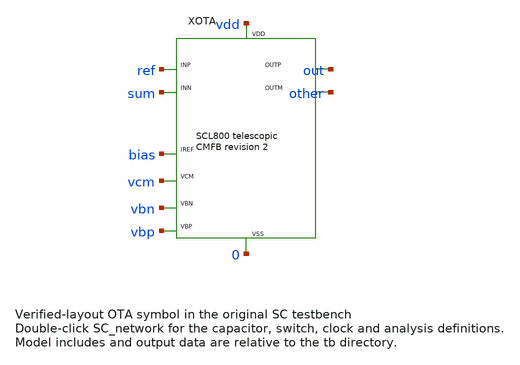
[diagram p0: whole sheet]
** sch_path: OTA/current_telescopic_cmfb_v2/designs/sc_ota_cmfb_v2.sch
**.subckt sc_ota_cmfb_v2
XOTA ref sum out other vdd 0 bias vcm vbn vbp ota_telescopic_cmfb_v2
**** begin user architecture code

.include /home/berson_meshak/pdk/scl08/ngspice_models49/mos/tntp49_5v
.include /home/berson_meshak/pdk/scl08/ngspice_models49/res/typ/ppr
.include ../models/ota_cmfb_v2_C.spice
.temp 27
.options reltol=1e-5 vntol=1e-8 abstol=1e-12 numdgt=12 method=gear maxord=2
VDD vdd 0 5
VREF ref 0 1.5
VP vp 0 0.3
IREF vdd bias 3.5u
CS tx rx 2.5p
CF sum out 7.5p
CL out 0 5p
VCM vcm 0 2.5
VBN vbn 0 2.4
VBP vbp vdd -2.2
COM other 0 5p
Vp1 p1 0 PWL(0 0 5.04e-05 0 5.041e-05 5 5.9e-05 5 5.901e-05 0 7.04e-05 0 7.041e-05 5 7.9e-05 5
+ 7.901e-05 0 9.04e-05 0 9.041e-05 5 9.9e-05 5 9.901e-05 0 0.0001304 0 0.00013041 5 0.000139 5 0.00013901 0
+ 0.0001504 0 0.00015041 5 0.000159 5 0.00015901 0 0.0001704 0 0.00017041 5 0.000179 5 0.00017901 0 0.00021 0)
Vp2 p2 0 PWL(0 0 6.04e-05 0 6.041e-05 5 6.9e-05 5 6.901e-05 0 8.04e-05 0 8.041e-05 5 8.9e-05 5
+ 8.901e-05 0 0.0001004 0 0.00010041 5 0.000109 5 0.00010901 0 0.0001404 0 0.00014041 5 0.000149 5 0.00014901 0
+ 0.0001604 0 0.00016041 5 0.000169 5 0.00016901 0 0.0001804 0 0.00018041 5 0.000189 5 0.00018901 0 0.00021 0)
Vrst rst 0 PWL(0 5 4.9e-05 5 4.901e-05 0 0.0001104 0 0.00011041 5 0.000129 5 0.00012901 0 0.00021 0)
Bp1b p1b 0 V=5-v(p1)
Bp2b p2b 0 V=5-v(p2)
Brstb rstb 0 V=5-v(rst)
MN0 tx p1 vp 0 N W=10u L=0.8u
MP0 tx p1b vp vdd P W=20u L=0.8u
MN1 tx p2 0 0 N W=10u L=0.8u
MP1 tx p2b 0 vdd P W=20u L=0.8u
MN2 rx p1 0 0 N W=10u L=0.8u
MP2 rx p1b 0 vdd P W=20u L=0.8u
MN3 rx p2 sum 0 N W=10u L=0.8u
MP3 rx p2b sum vdd P W=20u L=0.8u
MN4 sum rst out 0 N W=10u L=0.8u
MP4 sum rstb out vdd P W=20u L=0.8u
.control
set wr_singlescale
set wr_vecnames
tran 10n 0.00021
wrdata xschem_SC.dat v(out) v(sum) v(other) v(p1) v(p2) v(rst) i(vdd)
quit
.endc

**** end user architecture code
**.ends
.end
